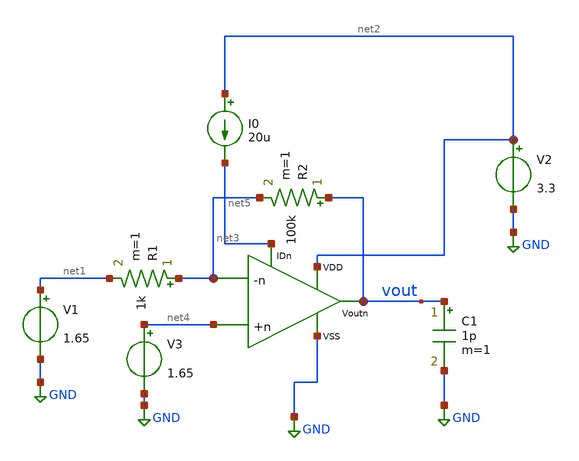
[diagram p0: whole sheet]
** sch_path: xschem/ota_miller/prueba.sch
**.subckt prueba
R1 net3 net1 1k m=1
R2 vout net3 100k m=1
V1 net1 GND 1.65
V2 net2 GND 3.3
C1 vout GND 1p m=1
V3 net4 GND 1.65
I0 net2 net5 20u
x1 net2 vout net5 net3 net4 GND ota_n_in
**** begin user architecture code


.control
save all
* Coloracion de graficas
set color0=white
set color1=black
set color2=blue
set color3=red
set xbrushwidth=2

* 1. Senoidales en contrafase (180 deg) con offset 1.65V, amplitud 1mV, frecuencia 1kHz
alter @v1[sin] [ 1.65 1m 1k 0 0 0 ]
alter @v3[sin] [ 1.65 1m 1k 0 0 180 ]

* 2. Simular 5 ms con paso de 1 us (5 ciclos de 1 kHz)
tran 1u 5m

* 3. Medir pico a pico directamente con meas (2ms a 5ms)
meas tran vout_pp pp v(vout) from=2m to=5m
meas tran vnet1_pp pp v(net1) from=2m to=5m

* 4. Calcular diferencia de entrada y su pico a pico en pasos separados
let vdiff = v(net4) - v(net1)
let vdiff_max = vecmax(vdiff)
let vdiff_min = vecmin(vdiff)
let vdiff_pp = vdiff_max - vdiff_min

* 5. Calcular ganancias por separado
let ganancia_v1 = vout_pp / vnet1_pp
let ganancia_diff = vout_pp / vdiff_pp

echo ========================================
print ganancia_v1
print ganancia_diff
echo ========================================

* 6. Graficar salida y entradas
plot v(vout) v(net1) v(net4) title 'Respuesta Transitoria OTA 5T' xlabel 'Tiempo (s)' ylabel 'Voltaje (V)'
.endc




.include /home/ringosinye/eda/pdks/gf180mcuD/libs.tech/ngspice/design.ngspice
.lib /home/ringosinye/eda/pdks/gf180mcuD/libs.tech/ngspice/sm141064.ngspice typical
.param sw_stat_mismatch = 0


**** end user architecture code
**.ends

* expanding   symbol:  ota_n_in.sym # of pins=6
** sym_path: xschem/ota_miller/ota_n_in.sym
** sch_path: xschem/ota_miller/ota_n_in.sch
.subckt ota_n_in VDD Voutn IDn -n +n VSS
*.opin Voutn
*.ipin VSS
*.ipin VDD
*.ipin +n
*.ipin -n
*.ipin IDn
XM1 net2 +n net1 GND nfet_03v3 L=1u W=4.1u nf=1 ad='int((nf+1)/2) * W/nf * 0.18u' as='int((nf+2)/2) * W/nf * 0.18u'
+ pd='2*int((nf+1)/2) * (W/nf + 0.18u)' ps='2*int((nf+2)/2) * (W/nf + 0.18u)' nrd='0.18u / W' nrs='0.18u / W'
+ sa=0 sb=0 sd=0 m=1 par=1
XM2 Voutn -n net1 GND nfet_03v3 L=1u W=4.1u nf=1 ad='int((nf+1)/2) * W/nf * 0.18u' as='int((nf+2)/2) * W/nf * 0.18u'
+ pd='2*int((nf+1)/2) * (W/nf + 0.18u)' ps='2*int((nf+2)/2) * (W/nf + 0.18u)' nrd='0.18u / W' nrs='0.18u / W'
+ sa=0 sb=0 sd=0 m=1 par=1
XM3 net2 net2 VDD VDD pfet_03v3 L=1u W=10u nf=1 ad='int((nf+1)/2) * W/nf * 0.18u' as='int((nf+2)/2) * W/nf * 0.18u'
+ pd='2*int((nf+1)/2) * (W/nf + 0.18u)' ps='2*int((nf+2)/2) * (W/nf + 0.18u)' nrd='0.18u / W' nrs='0.18u / W'
+ sa=0 sb=0 sd=0 m=1 par=1
XM4 Voutn net2 VDD VDD pfet_03v3 L=1u W=10u nf=1 ad='int((nf+1)/2) * W/nf * 0.18u' as='int((nf+2)/2) * W/nf * 0.18u'
+ pd='2*int((nf+1)/2) * (W/nf + 0.18u)' ps='2*int((nf+2)/2) * (W/nf + 0.18u)' nrd='0.18u / W' nrs='0.18u / W'
+ sa=0 sb=0 sd=0 m=1 par=1
XM5 net1 IDn VSS GND nfet_03v3 L=1u W=5u nf=1 ad='int((nf+1)/2) * W/nf * 0.18u' as='int((nf+2)/2) * W/nf * 0.18u'
+ pd='2*int((nf+1)/2) * (W/nf + 0.18u)' ps='2*int((nf+2)/2) * (W/nf + 0.18u)' nrd='0.18u / W' nrs='0.18u / W'
+ sa=0 sb=0 sd=0 m=1 par=1
XM6 IDn IDn VSS GND nfet_03v3 L=1u W=1u nf=1 ad='int((nf+1)/2) * W/nf * 0.18u' as='int((nf+2)/2) * W/nf * 0.18u'
+ pd='2*int((nf+1)/2) * (W/nf + 0.18u)' ps='2*int((nf+2)/2) * (W/nf + 0.18u)' nrd='0.18u / W' nrs='0.18u / W'
+ sa=0 sb=0 sd=0 m=1 par=1
.ends

.GLOBAL GND
.end
